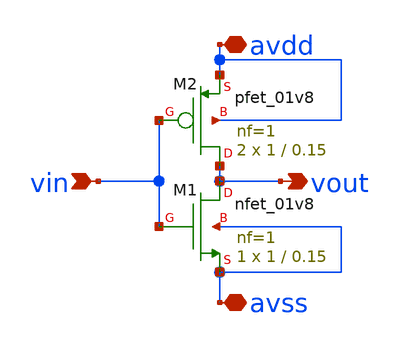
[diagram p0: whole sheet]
** sch_path: not.sch
**.subckt not vin vout avdd avss
*.ipin vin
*.opin vout
*.iopin avdd
*.iopin avss
XM1 vout vin avss avss sky130_fd_pr__nfet_01v8 L=0.15 W=1 nf=1 ad='int((1 + 1)/2) * 1 / 1 * 0.29' as='int((1 + 2)/2) * 1 / 1 * 0.29'
+ pd='2*int((1 + 1)/2) * (1 / 1 + 0.29)' ps='2*int((1 + 2)/2) * (1 / 1 + 0.29)' nrd='0.29 / 1 ' nrs='0.29 / 1 '
+ sa=0 sb=0 sd=0 mult=1 m=1
XM2 vout vin avdd avdd sky130_fd_pr__pfet_01v8 L=0.15 W=1 nf=1 ad='int((1 + 1)/2) * 1 / 1 * 0.29' as='int((1 + 2)/2) * 1 / 1 * 0.29'
+ pd='2*int((1 + 1)/2) * (1 / 1 + 0.29)' ps='2*int((1 + 2)/2) * (1 / 1 + 0.29)' nrd='0.29 / 1 ' nrs='0.29 / 1 '
+ sa=0 sb=0 sd=0 mult=2 m=2
**.ends
.end
